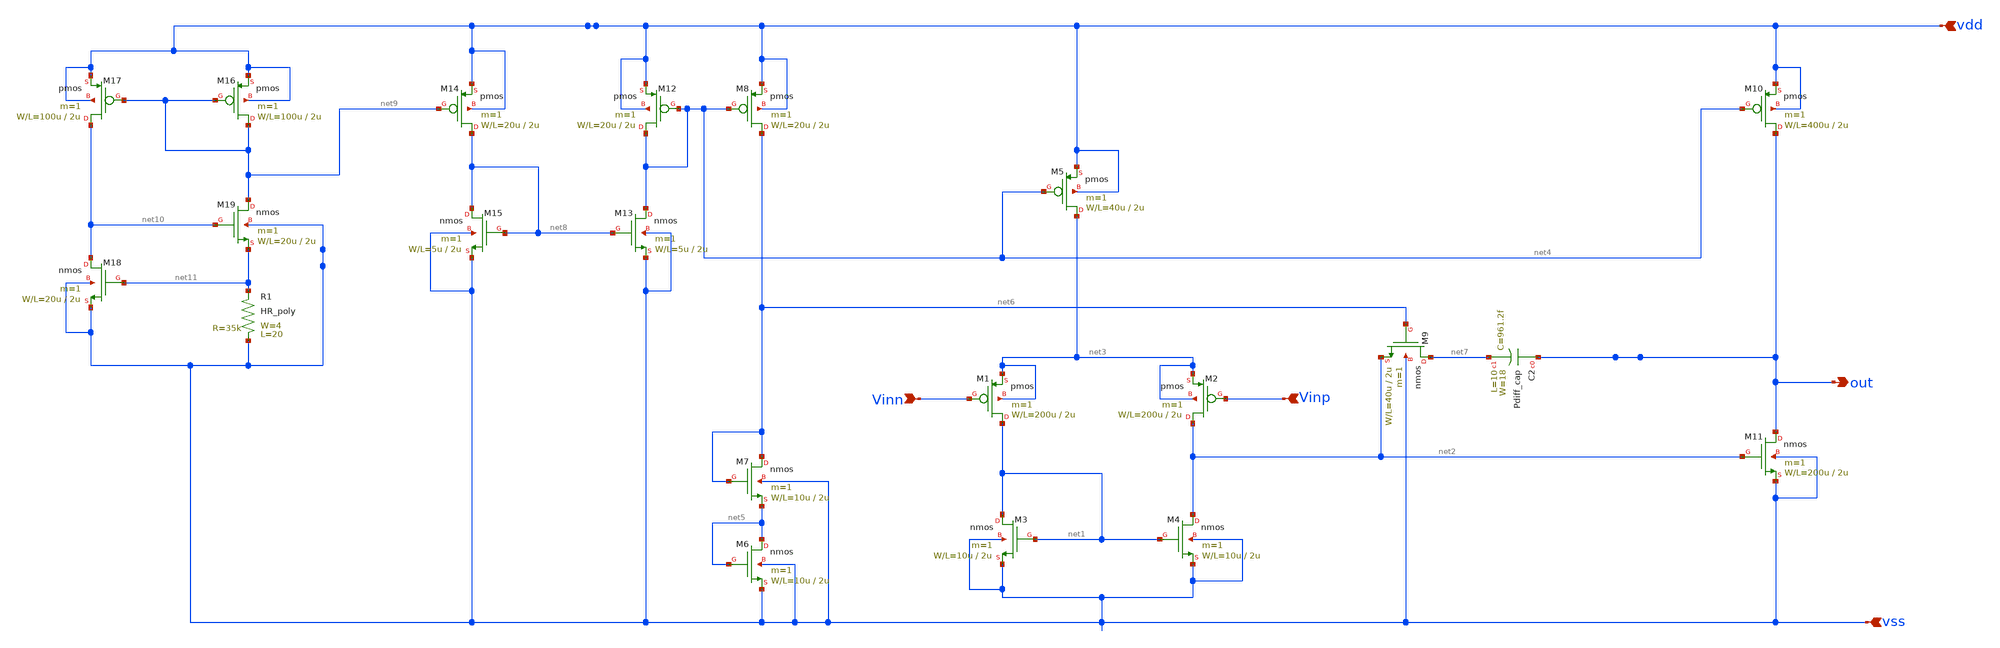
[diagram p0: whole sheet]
** sch_path: member_project/GroupWork/Team_Ando/foorests/circuit.sch
**.subckt circuit Vinn Vinp vdd out vss
*.ipin Vinn
*.ipin Vinp
*.ipin vdd
*.opin out
*.ipin vss
M1 net1 Vinn net3 net3 pmos L=2u W=200u m=1
M2 net2 Vinp net3 net3 pmos L=2u W=200u m=1
M3 net1 net1 vss vss nmos L=2u W=10u m=1
M4 net2 net1 vss vss nmos L=2u W=10u m=1
M5 net3 net4 vdd vdd pmos L=2u W=40u m=1
M6 net5 net5 vss vss nmos L=2u W=10u m=1
M7 net6 net6 net5 vss nmos L=2u W=10u m=1
M8 net6 net4 vdd vdd pmos L=2u W=20u m=1
M9 net7 net6 net2 vss nmos L=2u W=40u m=1
M10 out net4 vdd vdd pmos L=2u W=400u m=1
M11 out net2 vss vss nmos L=2u W=200u m=1
M12 net4 net4 vdd vdd pmos L=2u W=20u m=1
M13 net4 net8 vss vss nmos L=2u W=5u m=1
M14 net8 net9 vdd vdd pmos L=2u W=20u m=1
M15 net8 net8 vss vss nmos L=2u W=5u m=1
M16 net9 net9 vdd vdd pmos L=2u W=100u m=1
M17 net10 net9 vdd vdd pmos L=2u W=100u m=1
R1 vss net11 HR_poly W=4 L=20
M18 net10 net11 vss vss nmos L=2u W=20u m=1
M19 net9 net10 net11 vss nmos L=2u W=20u m=1
C2 out net7 Pdiff_cap W=18 L=10
**.ends
.end
